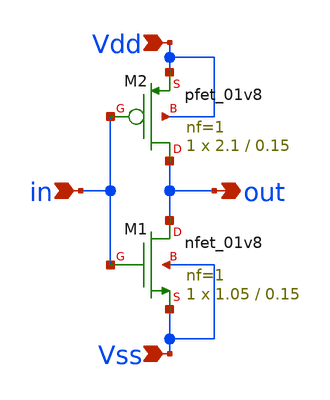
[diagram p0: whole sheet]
** sch_path: trabajosPracticos/tp6/archivosDelProfe/inversor/inversor.sch
**.subckt inversor in Vdd Vss out
*.ipin in
*.ipin Vdd
*.ipin Vss
*.opin out
XM1 out in Vss Vss sky130_fd_pr__nfet_01v8 L=0.15 W=1.05 nf=1 ad='int((nf+1)/2) * W/nf * 0.29' as='int((nf+2)/2) * W/nf * 0.29'
+ pd='2*int((nf+1)/2) * (W/nf + 0.29)' ps='2*int((nf+2)/2) * (W/nf + 0.29)' nrd='0.29 / W' nrs='0.29 / W'
+ sa=0 sb=0 sd=0 mult=1 m=1
XM2 out in Vdd Vdd sky130_fd_pr__pfet_01v8 L=0.15 W=2.1 nf=1 ad='int((nf+1)/2) * W/nf * 0.29' as='int((nf+2)/2) * W/nf * 0.29'
+ pd='2*int((nf+1)/2) * (W/nf + 0.29)' ps='2*int((nf+2)/2) * (W/nf + 0.29)' nrd='0.29 / W' nrs='0.29 / W'
+ sa=0 sb=0 sd=0 mult=1 m=1
**.ends
.end
